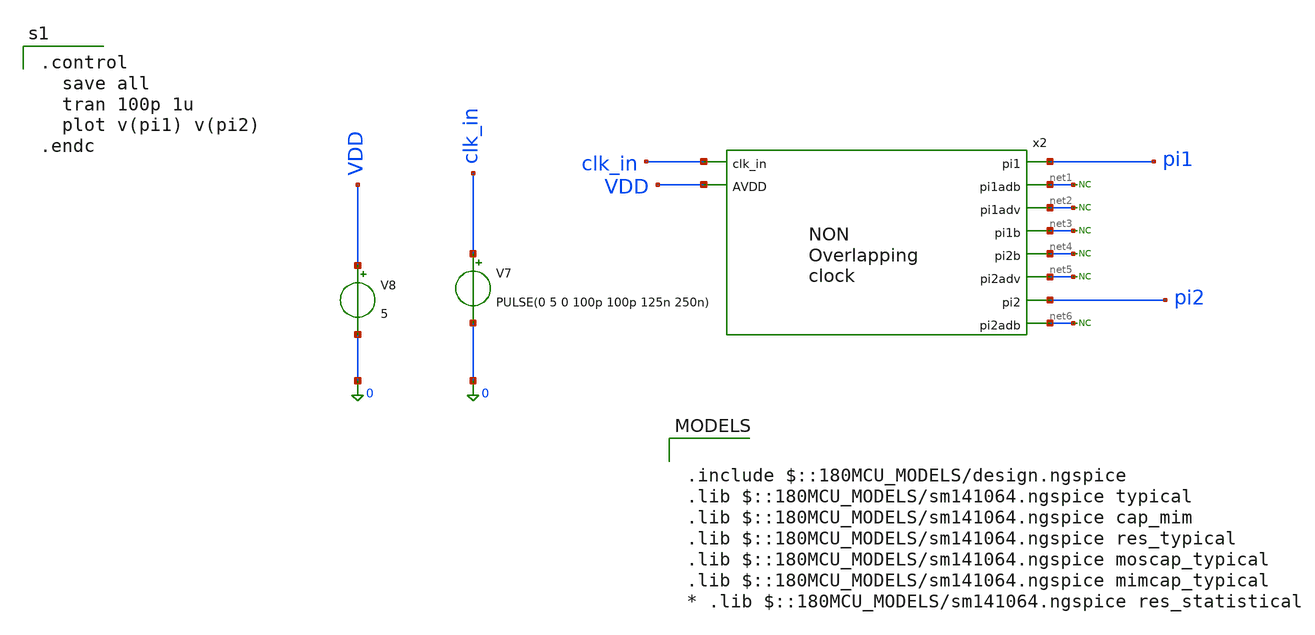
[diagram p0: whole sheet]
** sch_path: design/schematics/EIS/NOCG/tb_non_overlapping_clk.sch
**.subckt tb_non_overlapping_clk
x2 pi1 net1 net2 clk_in net3 VDD net4 net5 pi2 net6 SG_B11_cic_bms_afe_non_overlapping_clk
V7 clk_in 0 PULSE(0 5 0 100p 100p 125n 250n)
V8 VDD 0 5
* noconn #net1
* noconn #net2
* noconn #net3
* noconn #net4
* noconn #net5
* noconn #net6
**** begin user architecture code

.include $::180MCU_MODELS/design.ngspice
.lib $::180MCU_MODELS/sm141064.ngspice typical
.lib $::180MCU_MODELS/sm141064.ngspice cap_mim
.lib $::180MCU_MODELS/sm141064.ngspice res_typical
.lib $::180MCU_MODELS/sm141064.ngspice moscap_typical
.lib $::180MCU_MODELS/sm141064.ngspice mimcap_typical
* .lib $::180MCU_MODELS/sm141064.ngspice res_statistical


.control
  save all
  tran 100p 1u
  plot v(pi1) v(pi2)
.endc

**** end user architecture code
**.ends
.end
